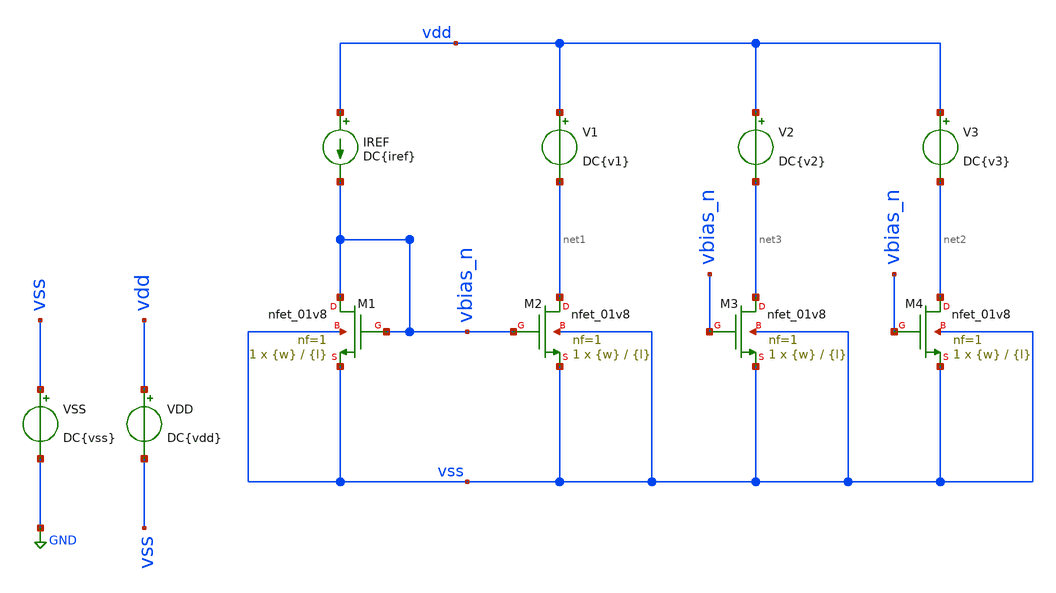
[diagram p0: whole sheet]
** sch_path: TP2/tp2_2.sch
**.subckt tp2_2
XM1 vbias_n vbias_n vss vss sky130_fd_pr__nfet_01v8 L={l} W={w} nf=1 ad='int((nf+1)/2) * W/nf * 0.29'
+ as='int((nf+2)/2) * W/nf * 0.29' pd='2*int((nf+1)/2) * (W/nf + 0.29)' ps='2*int((nf+2)/2) * (W/nf + 0.29)'
+ nrd='0.29 / W' nrs='0.29 / W' sa=0 sb=0 sd=0 mult=1 m=1
XM2 net1 vbias_n vss vss sky130_fd_pr__nfet_01v8 L={l} W={w} nf=1 ad='int((nf+1)/2) * W/nf * 0.29' as='int((nf+2)/2) * W/nf * 0.29'
+ pd='2*int((nf+1)/2) * (W/nf + 0.29)' ps='2*int((nf+2)/2) * (W/nf + 0.29)' nrd='0.29 / W' nrs='0.29 / W'
+ sa=0 sb=0 sd=0 mult=1 m=1
IREF vdd vbias_n DC{iref}
VSS vss GND DC{vss}
VDD vdd vss DC{vdd}
V2 vdd net3 DC{v2}
V3 vdd net2 DC{v3}
XM3 net3 vbias_n vss vss sky130_fd_pr__nfet_01v8 L={l} W={w} nf=1 ad='int((nf+1)/2) * W/nf * 0.29' as='int((nf+2)/2) * W/nf * 0.29'
+ pd='2*int((nf+1)/2) * (W/nf + 0.29)' ps='2*int((nf+2)/2) * (W/nf + 0.29)' nrd='0.29 / W' nrs='0.29 / W'
+ sa=0 sb=0 sd=0 mult=1 m=1
XM4 net2 vbias_n vss vss sky130_fd_pr__nfet_01v8 L={l} W={w} nf=1 ad='int((nf+1)/2) * W/nf * 0.29' as='int((nf+2)/2) * W/nf * 0.29'
+ pd='2*int((nf+1)/2) * (W/nf + 0.29)' ps='2*int((nf+2)/2) * (W/nf + 0.29)' nrd='0.29 / W' nrs='0.29 / W'
+ sa=0 sb=0 sd=0 mult=1 m=1
V1 vdd net1 DC{v1}
**** begin user architecture code



* Parameters
.param vdd = 1.8
.param vss = 0.0
.param v1 = 0.6
.param v2 = 0.9
.param v3 = 1.2
.param iref = 200u
.param w = 4.2
.param l = 0.15

* Models
.lib ~/skywater/skywater-pdk/libraries/sky130_fd_pr_ngspice/latest/models/corners/sky130.lib TT

* Data to save
.save all  @M.XM1.msky130_fd_pr__nfet_01v8[id]  @M.XM1.msky130_fd_pr__nfet_01v8[vth]  @M.XM1.msky130_fd_pr__nfet_01v8[vdsat]  @M.XM1.msky130_fd_pr__nfet_01v8[gm]  @M.XM1.msky130_fd_pr__nfet_01v8[vds]  @M.XM1.msky130_fd_pr__nfet_01v8[vgs]  @M.XM1.msky130_fd_pr__nfet_01v8[w]  @M.XM2.msky130_fd_pr__nfet_01v8[id]  @M.XM2.msky130_fd_pr__nfet_01v8[gm]  @M.XM2.msky130_fd_pr__nfet_01v8[vds]  @M.XM2.msky130_fd_pr__nfet_01v8[vgs]  @M.XM2.msky130_fd_pr__nfet_01v8[w]  @M.XM2.msky130_fd_pr__nfet_01v8[vdsat]  @M.XM2.msky130_fd_pr__nfet_01v8[vth]  @M.XM3.msky130_fd_pr__nfet_01v8[id]  @M.XM3.msky130_fd_pr__nfet_01v8[vth]  @M.XM3.msky130_fd_pr__nfet_01v8[vdsat]  @M.XM3.msky130_fd_pr__nfet_01v8[gm]  @M.XM3.msky130_fd_pr__nfet_01v8[vds]  @M.XM3.msky130_fd_pr__nfet_01v8[vgs]  @M.XM3.msky130_fd_pr__nfet_01v8[w]  @M.XM4.msky130_fd_pr__nfet_01v8[id]  @M.XM4.msky130_fd_pr__nfet_01v8[gm]  @M.XM4.msky130_fd_pr__nfet_01v8[vds]  @M.XM4.msky130_fd_pr__nfet_01v8[vgs]  @M.XM4.msky130_fd_pr__nfet_01v8[w]  @M.XM4.msky130_fd_pr__nfet_01v8[vdsat]  @M.XM4.msky130_fd_pr__nfet_01v8[vth]

* Simulation
.control
 * let wi = 4.2
  *let wf = 20
   *let wstep = 0.7

*  dowhile wi <= wf
 *   print @M.XM1.msky130_fd_pr__nfet_01v8[w]
  *  alter @M.XM1.msky130_fd_pr__nfet_01v8[w] = wi
  *  alter @M.XM2.msky130_fd_pr__nfet_01v8[w] = wi
  *  alter @M.XM3.msky130_fd_pr__nfet_01v8[w] = wi
  *  alter @M.XM4.msky130_fd_pr__nfet_01v8[w] = wi
  *  let wi = wi + wstep
  *  op
  *  print @M.XM1.msky130_fd_pr__nfet_01v8[w]
  *  print @M.XM1.msky130_fd_pr__nfet_01v8[l]
  *  print @M.XM1.msky130_fd_pr__nfet_01v8[id]
  *  print @M.XM1.msky130_fd_pr__nfet_01v8[vds]
  *  print @M.XM1.msky130_fd_pr__nfet_01v8[vgs]
  *  print @M.XM2.msky130_fd_pr__nfet_01v8[w]
  *  print @M.XM2.msky130_fd_pr__nfet_01v8[id]
  *  print @M.XM2.msky130_fd_pr__nfet_01v8[vds]
  *  print @M.XM2.msky130_fd_pr__nfet_01v8[vgs]
  *  print @M.XM3.msky130_fd_pr__nfet_01v8[w]
  *  print @M.XM3.msky130_fd_pr__nfet_01v8[id]
  *  print @M.XM3.msky130_fd_pr__nfet_01v8[vds]
  *  print @M.XM3.msky130_fd_pr__nfet_01v8[vgs]
  *  print @M.XM4.msky130_fd_pr__nfet_01v8[w]
  *  print @M.XM4.msky130_fd_pr__nfet_01v8[id]
  *  print @M.XM4.msky130_fd_pr__nfet_01v8[vds]
  *  print @M.XM4.msky130_fd_pr__nfet_01v8[vgs]
   * save all
  *end
  *write tp2_2.raw


  unset filetype
  op
  save all
  write tp2_2.raw

.endc

.end


**** end user architecture code
**.ends
.GLOBAL GND
.end
